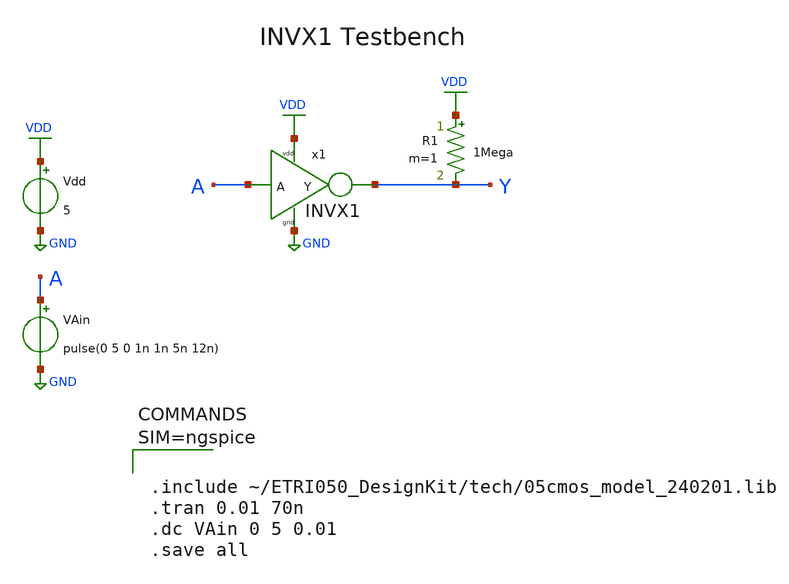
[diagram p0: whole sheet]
** sch_path: Tutorials/1-4_StdCell_DFFSR/Sch/INVX1_TB.sch
**.subckt INVX1_TB
Vdd VDD GND 5
VAin A GND pulse(0 5 0 1n 1n 5n 12n)
R1 VDD Y 1Mega m=1
x1 A Y VDD GND INVX1
**** begin user architecture code



.include ~/ETRI050_DesignKit/tech/05cmos_model_240201.lib
.tran 0.01 70n
.dc VAin 0 5 0.01
.save all



**** end user architecture code
**.ends

* expanding   symbol:  /home/goodkook/ETRI050_DesignKit/Tutorials/1-4_StdCell_DFFSR/Sch/INVX1.sym #
*+ of pins=4
** sym_path: Tutorials/1-4_StdCell_DFFSR/Sch/INVX1.sym
** sch_path: Tutorials/1-4_StdCell_DFFSR/Sch/INVX1.sch
.subckt INVX1 A Y vdd gnd
*.ipin A
*.opin Y
*.iopin vdd
*.iopin gnd
M1 Y A gnd GND nfet w=3u l=0.6u m=1
M2 Y A vdd VDD pfet w=6u l=0.6u m=1
.ends

.GLOBAL VDD
.GLOBAL GND
.end
